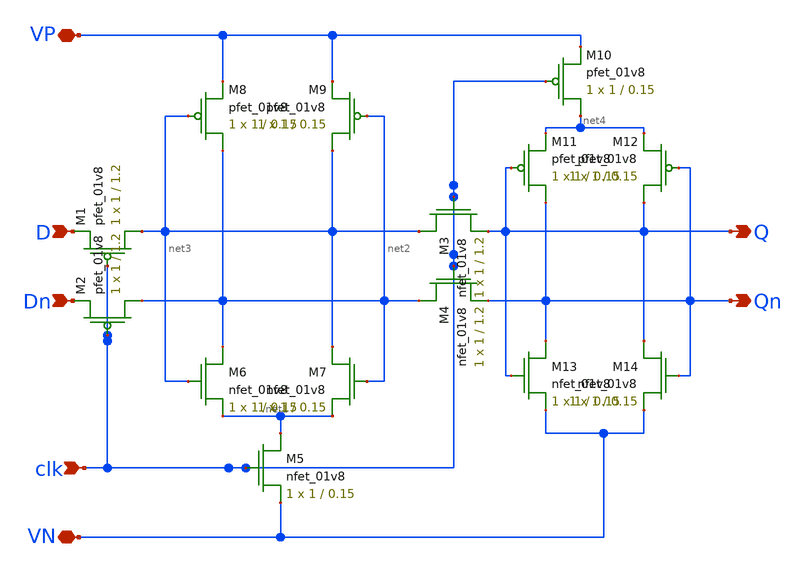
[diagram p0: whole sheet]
** sch_path: MiniProject2-CSRLDFF/XSCHEM/CSRLDFF.sch
**.subckt CSRLDFF D clk VN Q Qn Dn VP
*.ipin D
*.ipin clk
*.iopin VN
*.opin Q
*.opin Qn
*.ipin Dn
*.iopin VP
XM1 net3 clk D VDD sky130_fd_pr__pfet_01v8 L=1.2 W=1 nf=1 ad='int((nf+1)/2) * W/nf * 0.29' as='int((nf+2)/2) * W/nf * 0.29'
+ pd='2*int((nf+1)/2) * (W/nf + 0.29)' ps='2*int((nf+2)/2) * (W/nf + 0.29)' nrd='0.29 / W' nrs='0.29 / W'
+ sa=0 sb=0 sd=0 mult=1 m=1
XM2 net2 clk Dn VDD sky130_fd_pr__pfet_01v8 L=1.2 W=1 nf=1 ad='int((nf+1)/2) * W/nf * 0.29' as='int((nf+2)/2) * W/nf * 0.29'
+ pd='2*int((nf+1)/2) * (W/nf + 0.29)' ps='2*int((nf+2)/2) * (W/nf + 0.29)' nrd='0.29 / W' nrs='0.29 / W'
+ sa=0 sb=0 sd=0 mult=1 m=1
XM3 net3 clk Q GND sky130_fd_pr__nfet_01v8 L=1.2 W=1 nf=1 ad='int((nf+1)/2) * W/nf * 0.29' as='int((nf+2)/2) * W/nf * 0.29'
+ pd='2*int((nf+1)/2) * (W/nf + 0.29)' ps='2*int((nf+2)/2) * (W/nf + 0.29)' nrd='0.29 / W' nrs='0.29 / W'
+ sa=0 sb=0 sd=0 mult=1 m=1
XM4 net2 clk Qn GND sky130_fd_pr__nfet_01v8 L=1.2 W=1 nf=1 ad='int((nf+1)/2) * W/nf * 0.29' as='int((nf+2)/2) * W/nf * 0.29'
+ pd='2*int((nf+1)/2) * (W/nf + 0.29)' ps='2*int((nf+2)/2) * (W/nf + 0.29)' nrd='0.29 / W' nrs='0.29 / W'
+ sa=0 sb=0 sd=0 mult=1 m=1
XM5 net1 clk VN GND sky130_fd_pr__nfet_01v8 L=0.15 W=1 nf=1 ad='int((nf+1)/2) * W/nf * 0.29' as='int((nf+2)/2) * W/nf * 0.29'
+ pd='2*int((nf+1)/2) * (W/nf + 0.29)' ps='2*int((nf+2)/2) * (W/nf + 0.29)' nrd='0.29 / W' nrs='0.29 / W'
+ sa=0 sb=0 sd=0 mult=1 m=1
XM6 net2 net3 net1 GND sky130_fd_pr__nfet_01v8 L=0.15 W=1 nf=1 ad='int((nf+1)/2) * W/nf * 0.29' as='int((nf+2)/2) * W/nf * 0.29'
+ pd='2*int((nf+1)/2) * (W/nf + 0.29)' ps='2*int((nf+2)/2) * (W/nf + 0.29)' nrd='0.29 / W' nrs='0.29 / W'
+ sa=0 sb=0 sd=0 mult=1 m=1
XM7 net3 net2 net1 GND sky130_fd_pr__nfet_01v8 L=0.15 W=1 nf=1 ad='int((nf+1)/2) * W/nf * 0.29' as='int((nf+2)/2) * W/nf * 0.29'
+ pd='2*int((nf+1)/2) * (W/nf + 0.29)' ps='2*int((nf+2)/2) * (W/nf + 0.29)' nrd='0.29 / W' nrs='0.29 / W'
+ sa=0 sb=0 sd=0 mult=1 m=1
XM8 net2 net3 VP VDD sky130_fd_pr__pfet_01v8 L=0.15 W=1 nf=1 ad='int((nf+1)/2) * W/nf * 0.29' as='int((nf+2)/2) * W/nf * 0.29'
+ pd='2*int((nf+1)/2) * (W/nf + 0.29)' ps='2*int((nf+2)/2) * (W/nf + 0.29)' nrd='0.29 / W' nrs='0.29 / W'
+ sa=0 sb=0 sd=0 mult=1 m=1
XM9 net3 net2 VP VDD sky130_fd_pr__pfet_01v8 L=0.15 W=1 nf=1 ad='int((nf+1)/2) * W/nf * 0.29' as='int((nf+2)/2) * W/nf * 0.29'
+ pd='2*int((nf+1)/2) * (W/nf + 0.29)' ps='2*int((nf+2)/2) * (W/nf + 0.29)' nrd='0.29 / W' nrs='0.29 / W'
+ sa=0 sb=0 sd=0 mult=1 m=1
XM10 net4 clk VP VDD sky130_fd_pr__pfet_01v8 L=0.15 W=1 nf=1 ad='int((nf+1)/2) * W/nf * 0.29' as='int((nf+2)/2) * W/nf * 0.29'
+ pd='2*int((nf+1)/2) * (W/nf + 0.29)' ps='2*int((nf+2)/2) * (W/nf + 0.29)' nrd='0.29 / W' nrs='0.29 / W'
+ sa=0 sb=0 sd=0 mult=1 m=1
XM11 Qn Q net4 VDD sky130_fd_pr__pfet_01v8 L=0.15 W=1 nf=1 ad='int((nf+1)/2) * W/nf * 0.29' as='int((nf+2)/2) * W/nf * 0.29'
+ pd='2*int((nf+1)/2) * (W/nf + 0.29)' ps='2*int((nf+2)/2) * (W/nf + 0.29)' nrd='0.29 / W' nrs='0.29 / W'
+ sa=0 sb=0 sd=0 mult=1 m=1
XM12 Q Qn net4 VDD sky130_fd_pr__pfet_01v8 L=0.15 W=1 nf=1 ad='int((nf+1)/2) * W/nf * 0.29' as='int((nf+2)/2) * W/nf * 0.29'
+ pd='2*int((nf+1)/2) * (W/nf + 0.29)' ps='2*int((nf+2)/2) * (W/nf + 0.29)' nrd='0.29 / W' nrs='0.29 / W'
+ sa=0 sb=0 sd=0 mult=1 m=1
XM13 Qn Q VN GND sky130_fd_pr__nfet_01v8 L=0.15 W=1 nf=1 ad='int((nf+1)/2) * W/nf * 0.29' as='int((nf+2)/2) * W/nf * 0.29'
+ pd='2*int((nf+1)/2) * (W/nf + 0.29)' ps='2*int((nf+2)/2) * (W/nf + 0.29)' nrd='0.29 / W' nrs='0.29 / W'
+ sa=0 sb=0 sd=0 mult=1 m=1
XM14 Q Qn VN GND sky130_fd_pr__nfet_01v8 L=0.15 W=1 nf=1 ad='int((nf+1)/2) * W/nf * 0.29' as='int((nf+2)/2) * W/nf * 0.29'
+ pd='2*int((nf+1)/2) * (W/nf + 0.29)' ps='2*int((nf+2)/2) * (W/nf + 0.29)' nrd='0.29 / W' nrs='0.29 / W'
+ sa=0 sb=0 sd=0 mult=1 m=1
**.ends
.end
